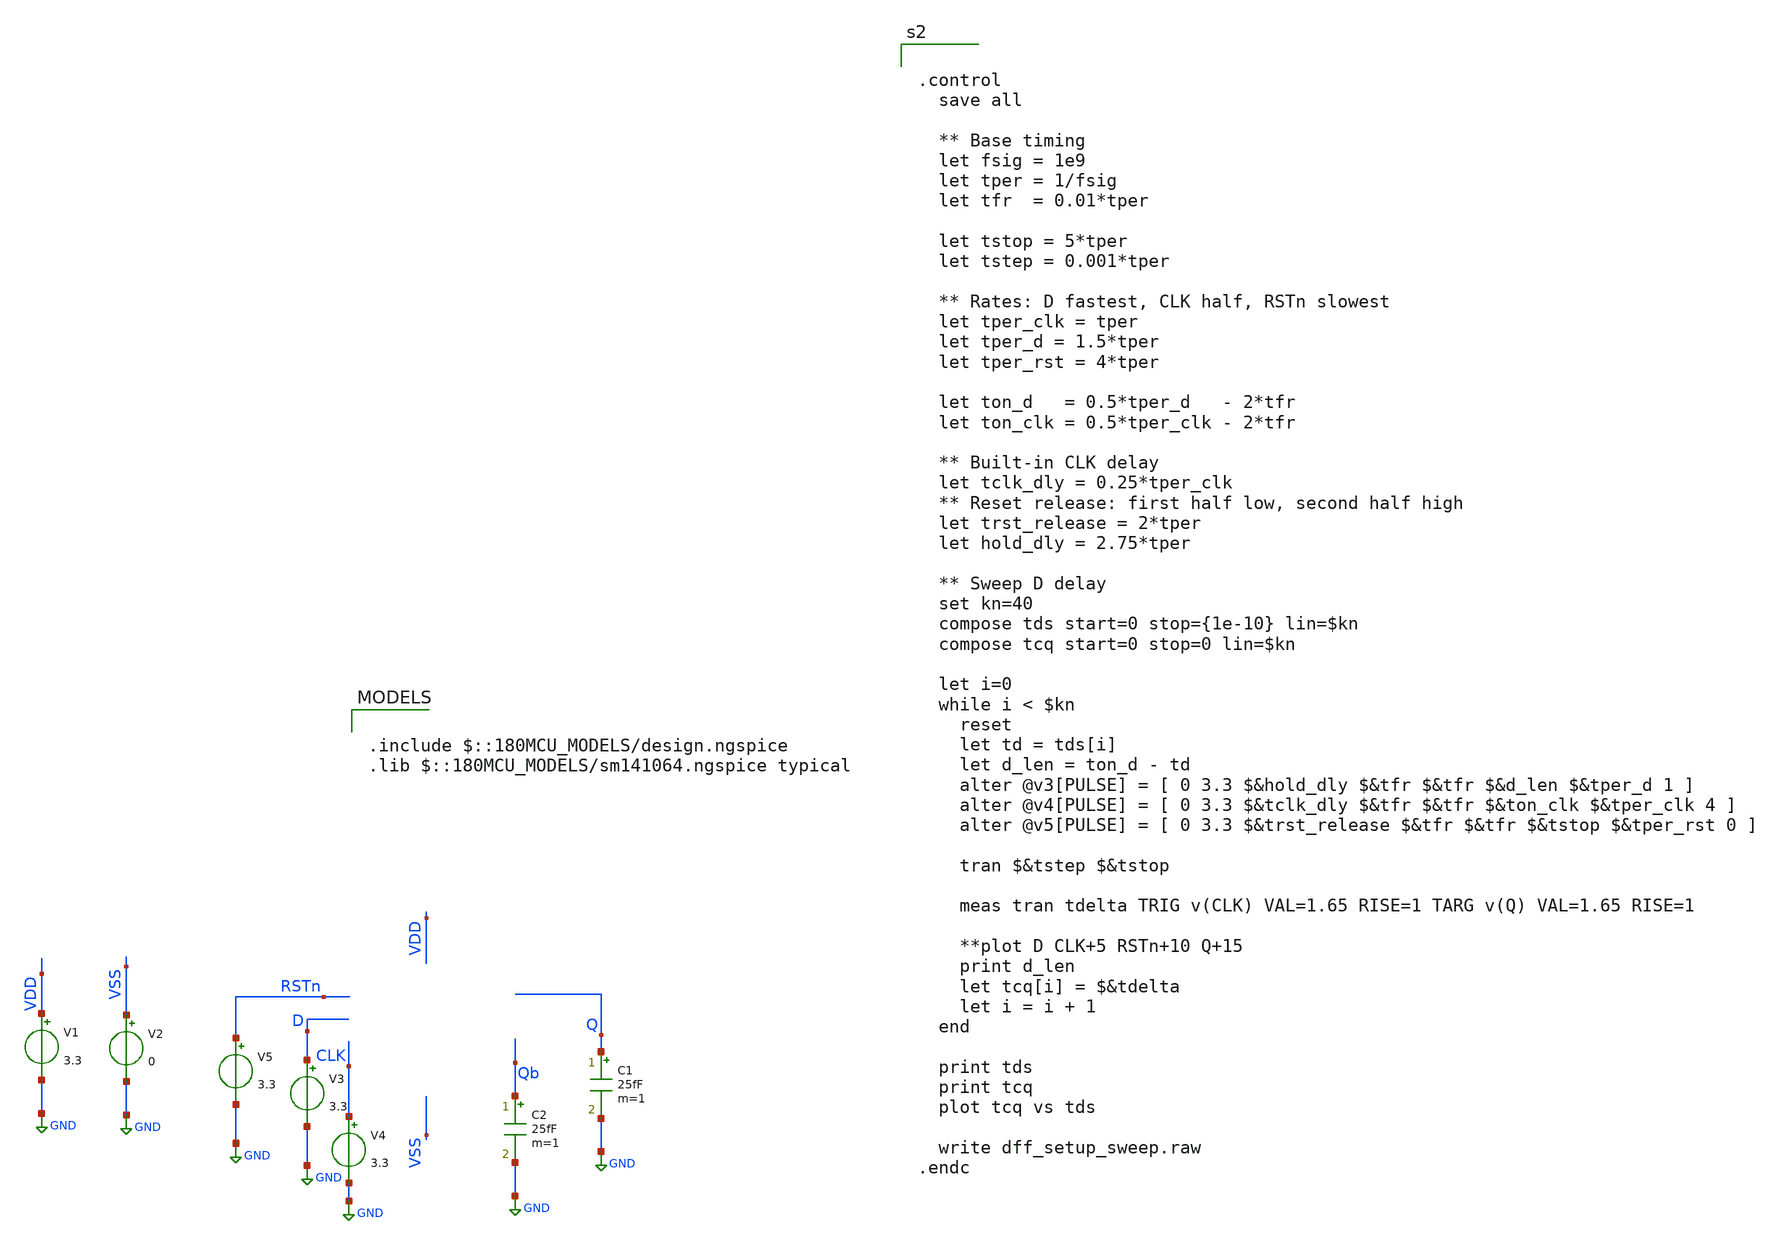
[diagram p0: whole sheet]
** sch_path: dff_postpex_hold.sch
**.subckt dff_postpex_hold
V1 VDD GND 3.3
V2 VSS GND 0
V3 D GND 3.3
C1 Q GND 25fF m=1
V4 CLK GND 3.3
C2 Qb GND 25fF m=1
V5 RSTn GND 3.3
**** begin user architecture code

.include $::180MCU_MODELS/design.ngspice
.lib $::180MCU_MODELS/sm141064.ngspice typical



.subckt dff_flat RSTN VDD CLK VSS D Q Qb
X0 a_n249_n4912# a_n1374_n6642# a_991_n4911# VSS.t1 nfet_03v3 ad=0.2646p pd=2.1u as=0.2646p ps=2.1u
+ w=0.42u l=0.28u
X1 VSS.t13 a_n359_n5759.t3 Q.t0 VSS.t12 nfet_03v3 ad=0.2646p pd=2.1u as=0.2646p ps=2.1u w=0.42u
+ l=0.28u
X2 a_n359_n5759.t1 a_n249_n4912# VDD.t17 VDD.t16 pfet_03v3 ad=0.1092p pd=0.94u as=0.2822p ps=2.18u
+ w=0.42u l=0.28u
X3 VDD.t15 RSTN.t0 a_881_n5758# VDD.t14 pfet_03v3 ad=0.2822p pd=2.18u as=0.1092p ps=0.94u w=0.42u
+ l=0.28u
X4 VDD.t3 a_n1374_n6642# a_1067_n6116# VDD.t2 pfet_03v3 ad=0.2822p pd=2.18u as=0.1092p ps=0.94u
+ w=0.42u l=0.28u
X5 a_2281_n4424# D.t0 a_1056_n4015# VSS.t11 nfet_03v3 ad=0.1092p pd=0.94u as=0.2646p ps=2.1u w=0.42u
+ l=0.28u
X6 VSS.t10 CLK.t0 a_n1342_n5730# VSS.t9 nfet_03v3 ad=0.2646p pd=2.1u as=0.2646p ps=2.1u w=0.42u
+ l=0.28u
X7 a_2280_n3998# D.t1 a_1056_n4015# VDD.t13 pfet_03v3 ad=0.1092p pd=0.94u as=0.2822p ps=2.18u
+ w=0.42u l=0.28u
X8 VDD.t19 CLK.t1 a_n1342_n5730# VDD.t18 pfet_03v3 ad=0.2822p pd=2.18u as=0.2822p ps=2.18u w=0.42u
+ l=0.28u
X9 VSS.t24 a_n1342_n5730# a_n1374_n6642# VSS.t23 nfet_03v3 ad=0.2667p pd=2.11u as=0.2625p ps=2.09u
+ w=0.42u l=0.28u
X10 a_1059_n5756# a_991_n4911# a_881_n5758# VSS.t25 nfet_03v3 ad=0.1092p pd=0.94u as=0.2646p ps=2.1u
+ w=0.42u l=0.28u
X11 VSS.t5 a_1056_n4015# a_991_n4911# VSS.t4 nfet_03v3 ad=0.2646p pd=2.1u as=0.2646p ps=2.1u w=0.42u
+ l=0.28u
X12 VSS.t22 a_n1342_n5730# a_1068_n6542# VSS.t21 nfet_03v3 ad=0.2646p pd=2.1u as=0.1092p ps=0.94u
+ w=0.42u l=0.28u
X13 VSS.t8 a_n912_n3722# Qb.t0 VSS.t7 nfet_03v3 ad=0.2646p pd=2.1u as=0.2646p ps=2.1u w=0.42u
+ l=0.28u
X14 VSS.t3 RSTN.t1 a_n181_n5757# VSS.t2 nfet_03v3 ad=0.2646p pd=2.1u as=0.1092p ps=0.94u w=0.42u
+ l=0.28u
X15 VDD.t12 a_n359_n5759.t4 Q.t1 VDD.t11 pfet_03v3 ad=0.2822p pd=2.18u as=0.2822p ps=2.18u w=0.42u
+ l=0.28u
X16 a_n249_n4912# a_n1342_n5730# a_991_n4911# VDD.t23 pfet_03v3 ad=0.2822p pd=2.18u as=0.2822p
+ ps=2.18u w=0.42u l=0.28u
X17 VSS.t16 a_n359_n5759.t5 a_n912_n3722# VSS.t15 nfet_03v3 ad=0.2646p pd=2.1u as=0.2646p ps=2.1u
+ w=0.42u l=0.28u
X18 VDD.t22 a_n1342_n5730# a_n1374_n6642# VDD.t21 pfet_03v3 ad=0.2822p pd=2.18u as=0.2822p ps=2.18u
+ w=0.42u l=0.28u
X19 a_881_n5758# a_n1374_n6642# a_1056_n4015# VSS.t0 nfet_03v3 ad=0.2646p pd=2.1u as=0.2646p ps=2.1u
+ w=0.42u l=0.28u
X20 VDD.t7 a_n912_n3722# Qb.t1 VDD.t6 pfet_03v3 ad=0.2822p pd=2.18u as=0.2822p ps=2.18u w=0.42u
+ l=0.28u
X21 VSS.t20 a_n1342_n5730# a_2281_n4424# VSS.t19 nfet_03v3 ad=0.2646p pd=2.1u as=0.1092p ps=0.94u
+ w=0.42u l=0.28u
X22 VDD.t27 RSTN.t2 a_n359_n5759.t2 VDD.t26 pfet_03v3 ad=0.2822p pd=2.18u as=0.1092p ps=0.94u
+ w=0.42u l=0.28u
X23 VDD.t1 a_n1374_n6642# a_2280_n3998# VDD.t0 pfet_03v3 ad=0.2822p pd=2.18u as=0.1092p ps=0.94u
+ w=0.42u l=0.28u
X24 a_1067_n6116# a_n359_n5759.t6 a_n249_n4912# VDD.t10 pfet_03v3 ad=0.1092p pd=0.94u as=0.2822p
+ ps=2.18u w=0.42u l=0.28u
X25 a_881_n5758# a_991_n4911# VDD.t25 VDD.t24 pfet_03v3 ad=0.1092p pd=0.94u as=0.2822p ps=2.18u
+ w=0.42u l=0.28u
X26 VSS.t18 RSTN.t3 a_1059_n5756# VSS.t17 nfet_03v3 ad=0.2646p pd=2.1u as=0.1092p ps=0.94u w=0.42u
+ l=0.28u
X27 VDD.t5 a_1056_n4015# a_991_n4911# VDD.t4 pfet_03v3 ad=0.2822p pd=2.18u as=0.2822p ps=2.18u
+ w=0.42u l=0.28u
X28 a_881_n5758# a_n1342_n5730# a_1056_n4015# VDD.t20 pfet_03v3 ad=0.2822p pd=2.18u as=0.2822p
+ ps=2.18u w=0.42u l=0.28u
X29 a_1068_n6542# a_n359_n5759.t7 a_n249_n4912# VSS.t6 nfet_03v3 ad=0.1092p pd=0.94u as=0.2646p
+ ps=2.1u w=0.42u l=0.28u
X30 a_n181_n5757# a_n249_n4912# a_n359_n5759.t0 VSS.t14 nfet_03v3 ad=0.1092p pd=0.94u as=0.2646p
+ ps=2.1u w=0.42u l=0.28u
X31 VDD.t9 a_n359_n5759.t8 a_n912_n3722# VDD.t8 pfet_03v3 ad=0.2822p pd=2.18u as=0.2822p ps=2.18u
+ w=0.42u l=0.28u
R0 VSS.n23 VSS.n16 749278
R1 VSS.n16 VSS.t11 91327.6
R2 VSS.n5 VSS.n3 64653.5
R3 VSS.n50 VSS.n3 47027.8
R4 VSS.n13 VSS.n8 11150.5
R5 VSS.t7 VSS.n46 10656.3
R6 VSS.n46 VSS.n45 9310.54
R7 VSS.n6 VSS.n3 9172.39
R8 VSS.n17 VSS.n8 8859.18
R9 VSS.n46 VSS.n7 7710.44
R10 VSS.n43 VSS.n9 6769.51
R11 VSS.n35 VSS.n34 6625.47
R12 VSS.n45 VSS.n8 5874.35
R13 VSS.t23 VSS.n49 4464.13
R14 VSS.n13 VSS.n11 4354.26
R15 VSS.n30 VSS.n10 4226.8
R16 VSS.n29 VSS.n11 4102.23
R17 VSS.n45 VSS.n44 3676.98
R18 VSS.n24 VSS.n23 3564.92
R19 VSS.n44 VSS.t0 2894.81
R20 VSS.n47 VSS.n7 2588.74
R21 VSS.t12 VSS.n3 2474.65
R22 VSS.n49 VSS.n48 2224.45
R23 VSS.n49 VSS.t9 1774.36
R24 VSS.n48 VSS.n6 1755.92
R25 VSS.n22 VSS.n21 1702.15
R26 VSS.t4 VSS.n24 1689.9
R27 VSS.n24 VSS.n10 1589.78
R28 VSS.t9 VSS.n5 1493.57
R29 VSS.t19 VSS.n15 1430.46
R30 VSS.n25 VSS.t4 1413.04
R31 VSS.t25 VSS.n9 1360.03
R32 VSS.n21 VSS.t0 1205.49
R33 VSS.t15 VSS.n7 1196.19
R34 VSS.n48 VSS.n47 1177.13
R35 VSS.n18 VSS.t17 1172.44
R36 VSS.n23 VSS.n22 1095.11
R37 VSS.n25 VSS.n11 1090.87
R38 VSS.n36 VSS.t2 1070.49
R39 VSS.n34 VSS.t6 1055.67
R40 VSS.n42 VSS.t15 992.063
R41 VSS.n30 VSS.t1 940.115
R42 VSS.n50 VSS.t23 920.712
R43 VSS.t11 VSS.t19 915.494
R44 VSS.n18 VSS.n10 900.433
R45 VSS.n34 VSS.n33 836.077
R46 VSS.n36 VSS.n35 822.135
R47 VSS.n32 VSS.n30 797.649
R48 VSS.t17 VSS.t25 750.361
R49 VSS.t2 VSS.t14 685.112
R50 VSS.n17 VSS.n16 674.74
R51 VSS.n38 VSS.n7 671.655
R52 VSS.n43 VSS.n42 615.08
R53 VSS.n33 VSS.t12 604.99
R54 VSS.t21 VSS.n32 576.241
R55 VSS.t1 VSS.n29 492.724
R56 VSS.n44 VSS.n43 472.2
R57 VSS.n15 VSS.n13 469.19
R58 VSS.t14 VSS.n6 466.733
R59 VSS.n47 VSS.t7 415.238
R60 VSS.t6 VSS.t21 368.795
R61 VSS.n35 VSS.n9 317.529
R62 VSS.n22 VSS.n17 57.864
R63 VSS.n21 VSS.n20 15.3475
R64 VSS.n51 VSS.t24 12.5437
R65 VSS.n37 VSS.t3 12.4687
R66 VSS.n31 VSS.t22 12.4687
R67 VSS.n19 VSS.t18 12.4687
R68 VSS.n26 VSS.t5 12.4687
R69 VSS.n41 VSS.t16 12.4687
R70 VSS.n4 VSS.t10 12.4687
R71 VSS.n1 VSS.t13 12.4687
R72 VSS.n38 VSS.t8 12.4687
R73 VSS.n14 VSS.t20 12.4675
R74 VSS.n29 VSS.n28 11.6695
R75 VSS.n15 VSS.n14 10.4017
R76 VSS.n19 VSS.n18 10.4005
R77 VSS.n26 VSS.n25 10.4005
R78 VSS.n5 VSS.n4 10.4005
R79 VSS.n33 VSS.n1 10.4005
R80 VSS.n51 VSS.n50 10.4005
R81 VSS.n42 VSS.n41 10.4005
R82 VSS.n32 VSS.n31 10.4005
R83 VSS.n37 VSS.n36 10.4005
R84 VSS.n31 VSS.n0 9.86036
R85 VSS.n28 VSS.n27 6.42418
R86 VSS.n20 VSS.n19 6.02652
R87 VSS.n39 VSS.n38 5.75457
R88 VSS.n39 VSS.n2 5.48837
R89 VSS.n41 VSS.n40 5.44665
R90 VSS.n40 VSS.n37 5.3877
R91 VSS.n27 VSS.n26 4.66984
R92 VSS.n14 VSS.n12 4.6547
R93 VSS.n20 VSS.n12 1.34731
R94 VSS.n40 VSS.n39 1.2245
R95 VSS.n27 VSS.n12 1.03428
R96 VSS.n52 VSS.n2 0.820259
R97 VSS VSS.n0 0.783577
R98 VSS.n28 VSS.n0 0.664346
R99 VSS.n53 VSS.n52 0.652808
R100 VSS VSS.n53 0.348192
R101 VSS.n4 VSS.n2 0.323682
R102 VSS.n53 VSS.n1 0.322765
R103 VSS.n52 VSS.n51 0.314599
R104 a_n359_n5759.t8 a_n359_n5759.t5 69.3505
R105 a_n359_n5759.t4 a_n359_n5759.t3 69.3505
R106 a_n359_n5759.t6 a_n359_n5759.t7 53.4469
R107 a_n359_n5759.n2 a_n359_n5759.t6 35.2609
R108 a_n359_n5759.n1 a_n359_n5759.t8 30.3133
R109 a_n359_n5759.n2 a_n359_n5759.t4 25.048
R110 a_n359_n5759.t0 a_n359_n5759.n3 12.3005
R111 a_n359_n5759.n1 a_n359_n5759.n0 5.78668
R112 a_n359_n5759.n0 a_n359_n5759.t2 4.33383
R113 a_n359_n5759.n0 a_n359_n5759.t1 4.33383
R114 a_n359_n5759.n3 a_n359_n5759.n2 0.519935
R115 a_n359_n5759.n3 a_n359_n5759.n1 0.494983
R116 Q Q.t0 12.6202
R117 Q Q.t1 12.341
R118 VDD.n8 VDD.t23 715.11
R119 VDD.n11 VDD.t20 714.49
R120 VDD.n18 VDD.t21 713.694
R121 VDD.n14 VDD.t6 713.688
R122 VDD.n17 VDD.t18 713.688
R123 VDD.n12 VDD.t26 713.688
R124 VDD.n16 VDD.t8 713.688
R125 VDD.n9 VDD.t0 713.688
R126 VDD.n6 VDD.t4 713.688
R127 VDD.n0 VDD.t14 713.688
R128 VDD.n3 VDD.t2 713.688
R129 VDD.n2 VDD.t11 713.688
R130 VDD.t26 VDD.t16 434.784
R131 VDD.t0 VDD.t13 434.784
R132 VDD.t14 VDD.t24 434.784
R133 VDD.t2 VDD.t10 434.784
R134 VDD.n0 VDD.t25 13.7623
R135 VDD.n13 VDD.t17 12.5331
R136 VDD.n17 VDD.t19 12.1992
R137 VDD.n16 VDD.t9 12.1992
R138 VDD.n6 VDD.t5 12.1992
R139 VDD.n3 VDD.t3 12.1992
R140 VDD.n2 VDD.t12 12.1992
R141 VDD.n14 VDD.t7 12.198
R142 VDD.n10 VDD.t1 12.1968
R143 VDD.n18 VDD.t22 12.192
R144 VDD.n12 VDD.t27 12.1422
R145 VDD.n1 VDD.t15 12.1411
R146 VDD.n19 VDD.n18 11.4596
R147 VDD.n16 VDD.n15 9.90617
R148 VDD.n4 VDD.n2 7.0573
R149 VDD.n7 VDD.n5 5.46986
R150 VDD.n5 VDD.n1 5.05424
R151 VDD.n4 VDD.n3 5.0066
R152 VDD.n20 VDD.n19 3.429
R153 VDD.n11 VDD.n10 1.6793
R154 VDD.n19 VDD.n17 1.5236
R155 VDD.n9 VDD.n8 1.27962
R156 VDD.n13 VDD.n12 1.1387
R157 VDD VDD.n11 0.864995
R158 VDD.n5 VDD.n4 0.845079
R159 VDD.n20 VDD.n16 0.527474
R160 VDD.n15 VDD.n14 0.516611
R161 VDD.n15 VDD.n13 0.457423
R162 VDD.n8 VDD.n7 0.351026
R163 VDD VDD.n20 0.00545413
R164 VDD.n10 VDD.n9 0.00286842
R165 VDD.n7 VDD.n6 0.00168421
R166 VDD.n1 VDD.n0 0.00153448
R167 RSTN.t0 RSTN.t3 89.2951
R168 RSTN.t2 RSTN.t1 89.2951
R169 RSTN.n0 RSTN.t2 44.9198
R170 RSTN.n0 RSTN.t0 24.9469
R171 RSTN RSTN.n0 0.00286842
R172 D.t1 D.t0 53.4469
R173 D D.t1 24.9505
R174 CLK.t1 CLK.t0 69.3505
R175 CLK CLK.t1 24.9517
R176 Qb Qb.t0 12.6395
R177 Qb Qb.t1 12.3217
C0 VDD a_n1342_n5730# 1.71536f
C1 a_n249_n4912# a_881_n5758# 0.19693f
C2 a_n1374_n6642# a_n1342_n5730# 1.67868f
C3 RSTN a_n249_n4912# 0.28644f
C4 a_n249_n4912# a_n1342_n5730# 0.21283f
C5 a_1056_n4015# a_881_n5758# 0.25267f
C6 VDD a_991_n4911# 0.76938f
C7 a_881_n5758# a_n1342_n5730# 0.31376f
C8 a_n1374_n6642# a_991_n4911# 0.22275f
C9 VDD D 0.18707f
C10 VDD a_n912_n3722# 0.83176f
C11 a_n249_n4912# a_991_n4911# 0.11019f
C12 VDD CLK 0.28794f
C13 VDD a_n1374_n6642# 1.886f
C14 VDD a_n249_n4912# 0.56511f
C15 a_991_n4911# a_881_n5758# 0.35092f
C16 a_n1374_n6642# a_n249_n4912# 0.23084f
C17 a_1056_n4015# a_991_n4911# 0.10365f
C18 VDD a_881_n5758# 1.18904f
C19 RSTN a_991_n4911# 0.29193f
C20 VDD a_1056_n4015# 0.95856f
C21 a_n1374_n6642# a_881_n5758# 0.24946f
C22 VDD Qb 0.10704f
C23 VDD RSTN 0.80322f
C24 a_n1374_n6642# a_1056_n4015# 0.2678f
C25 Q VSS 0.25589f
C26 CLK VSS 0.39888f
C27 RSTN VSS 1.32962f
C28 D VSS 0.27844f
C29 Qb VSS 0.15428f
C30 VDD VSS 18.83505f
C31 a_991_n4911# VSS 1.33038f
C32 a_n249_n4912# VSS 2.53842f
C33 a_881_n5758# VSS 0.89126f
C34 a_1056_n4015# VSS 1.26966f
C35 a_n1374_n6642# VSS 5.44569f
C36 a_n1342_n5730# VSS 6.88765f
C37 a_n912_n3722# VSS 0.62392f
C38 VDD.n8 VSS 0.11133f
C39 VDD.n11 VSS 0.13113f
C40 VDD.n19 VSS 0.21025f
C41 VDD.n20 VSS 0.10843f
C42 a_n359_n5759.t8 VSS 0.19196f
C43 a_n359_n5759.n1 VSS 1.35777f
C44 a_n359_n5759.t6 VSS 0.11284f
C45 a_n359_n5759.n2 VSS 0.45569f
C46 a_n359_n5759.n3 VSS 0.14466f
.ends

X0 RSTN VDD CLK VSS D Q Qb dff_flat




.control
  save all

  ** Base timing
  let fsig = 1e9
  let tper = 1/fsig
  let tfr  = 0.01*tper

  let tstop = 5*tper
  let tstep = 0.001*tper

  ** Rates: D fastest, CLK half, RSTn slowest
  let tper_clk = tper
  let tper_d = 1.5*tper
  let tper_rst = 4*tper

  let ton_d   = 0.5*tper_d   - 2*tfr
  let ton_clk = 0.5*tper_clk - 2*tfr

  ** Built-in CLK delay
  let tclk_dly = 0.25*tper_clk
  ** Reset release: first half low, second half high
  let trst_release = 2*tper
  let hold_dly = 2.75*tper

  ** Sweep D delay
  set kn=40
  compose tds start=0 stop={1e-10} lin=$kn
  compose tcq start=0 stop=0 lin=$kn

  let i=0
  while i < $kn
    reset
    let td = tds[i]
    let d_len = ton_d - td
    alter @v3[PULSE] = [ 0 3.3 $&hold_dly $&tfr $&tfr $&d_len $&tper_d 1 ]
    alter @v4[PULSE] = [ 0 3.3 $&tclk_dly $&tfr $&tfr $&ton_clk $&tper_clk 4 ]
    alter @v5[PULSE] = [ 0 3.3 $&trst_release $&tfr $&tfr $&tstop $&tper_rst 0 ]

    tran $&tstep $&tstop

    meas tran tdelta TRIG v(CLK) VAL=1.65 RISE=1 TARG v(Q) VAL=1.65 RISE=1

    **plot D CLK+5 RSTn+10 Q+15
    print d_len
    let tcq[i] = $&tdelta
    let i = i + 1
  end

  print tds
  print tcq
  plot tcq vs tds

  write dff_setup_sweep.raw
.endc


**** end user architecture code
**.ends
.GLOBAL GND
.end
